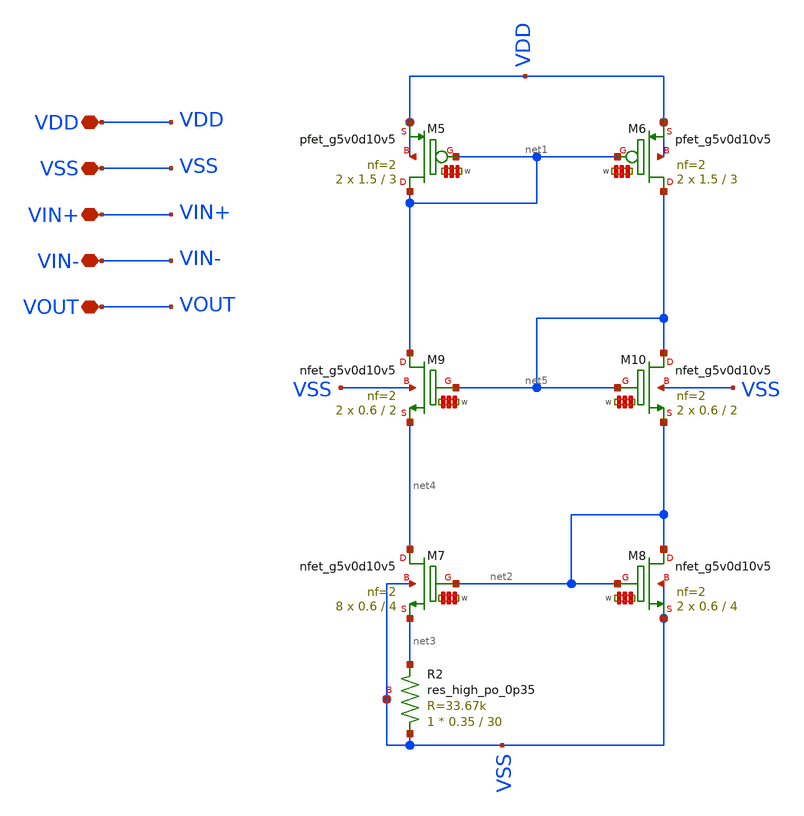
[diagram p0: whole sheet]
** sch_path: LIB/Sky130A/single ended amplifiers/VA001_pmos_5_sky130A.sch
**.subckt VA001_pmos_5_sky130A VDD VSS VIN+ VIN- VOUT
*.iopin VDD
*.iopin VSS
*.iopin VIN+
*.iopin VIN-
*.iopin VOUT
XM5 net1 net1 VDD VDD sky130_fd_pr__pfet_g5v0d10v5 L=3 W='1.5 * 2 ' nf=2 ad='int((2 + 1)/2) * 1.5 * 0.29'
+ as='int((2 + 2)/2) * 1.5 * 0.29' pd='2*int((2 + 1)/2) * (1.5 + 0.29)' ps='2*int((2 + 2)/2) * (1.5 + 0.29)'
+ nrd='0.29 / 1.5 / 2 ' nrs='0.29 / 1.5 / 2 ' sa=0 sb=0 sd=0 mult=2 m=2
XM6 net5 net1 VDD VDD sky130_fd_pr__pfet_g5v0d10v5 L=3 W='1.5 * 2 ' nf=2 ad='int((2 + 1)/2) * 1.5 * 0.29'
+ as='int((2 + 2)/2) * 1.5 * 0.29' pd='2*int((2 + 1)/2) * (1.5 + 0.29)' ps='2*int((2 + 2)/2) * (1.5 + 0.29)'
+ nrd='0.29 / 1.5 / 2 ' nrs='0.29 / 1.5 / 2 ' sa=0 sb=0 sd=0 mult=2 m=2
XM7 net4 net2 net3 VSS sky130_fd_pr__nfet_g5v0d10v5 L=4 W='0.6 * 2 ' nf=2 ad='int((nf+1)/2) * W / nf * 0.29'
+ as='int((nf+2)/2) * W / nf * 0.29' pd='2*int((nf+1)/2) * (W / nf + 0.29)' ps='2*int((nf+2)/2) * (W / nf + 0.29)'
+ nrd='0.29 / W ' nrs='0.29 / W ' sa=0 sb=0 sd=0 mult=8 m=8
XM8 net2 net2 VSS VSS sky130_fd_pr__nfet_g5v0d10v5 L=4 W='0.6 * 2 ' nf=2 ad='int((nf+1)/2) * W / nf * 0.29'
+ as='int((nf+2)/2) * W / nf * 0.29' pd='2*int((nf+1)/2) * (W / nf + 0.29)' ps='2*int((nf+2)/2) * (W / nf + 0.29)'
+ nrd='0.29 / W ' nrs='0.29 / W ' sa=0 sb=0 sd=0 mult=2 m=2
XM9 net1 net5 net4 VSS sky130_fd_pr__nfet_g5v0d10v5 L=2 W='0.6 * 2 ' nf=2 ad='int((nf+1)/2) * W / nf * 0.29'
+ as='int((nf+2)/2) * W / nf * 0.29' pd='2*int((nf+1)/2) * (W / nf + 0.29)' ps='2*int((nf+2)/2) * (W / nf + 0.29)'
+ nrd='0.29 / W ' nrs='0.29 / W ' sa=0 sb=0 sd=0 mult=2 m=2
XM10 net5 net5 net2 VSS sky130_fd_pr__nfet_g5v0d10v5 L=2 W='0.6 * 2 ' nf=2 ad='int((nf+1)/2) * W / nf * 0.29'
+ as='int((nf+2)/2) * W / nf * 0.29' pd='2*int((nf+1)/2) * (W / nf + 0.29)' ps='2*int((nf+2)/2) * (W / nf + 0.29)'
+ nrd='0.29 / W ' nrs='0.29 / W ' sa=0 sb=0 sd=0 mult=2 m=2
XR2 VSS net3 VSS sky130_fd_pr__res_high_po_0p35 L=30 mult=1 m=1
**.ends
.end
